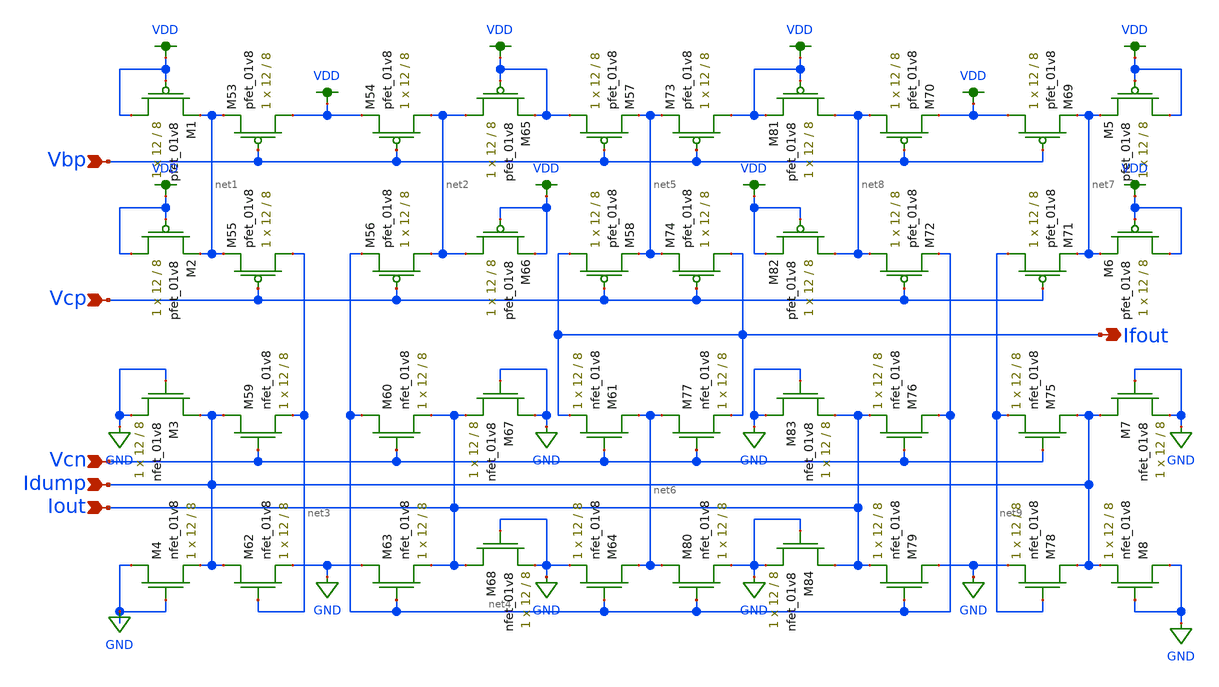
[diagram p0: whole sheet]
** sch_path: xschem/old_files/fvf.sch
**.subckt fvf Vbp Vcp Vcn Ifout Idump Iout
*.ipin Vbp
*.ipin Vcp
*.ipin Vcn
*.opin Ifout
*.ipin Idump
*.ipin Iout
XM53 VDD Vbp net1 VDD sky130_fd_pr__pfet_01v8 L=8 W=12 nf=1 ad='int((nf+1)/2) * W/nf * 0.29' as='int((nf+2)/2) * W/nf * 0.29'
+ pd='2*int((nf+1)/2) * (W/nf + 0.29)' ps='2*int((nf+2)/2) * (W/nf + 0.29)' nrd='0.29 / W' nrs='0.29 / W'
+ sa=0 sb=0 sd=0 mult=1 m=1
XM54 net2 Vbp VDD VDD sky130_fd_pr__pfet_01v8 L=8 W=12 nf=1 ad='int((nf+1)/2) * W/nf * 0.29' as='int((nf+2)/2) * W/nf * 0.29'
+ pd='2*int((nf+1)/2) * (W/nf + 0.29)' ps='2*int((nf+2)/2) * (W/nf + 0.29)' nrd='0.29 / W' nrs='0.29 / W'
+ sa=0 sb=0 sd=0 mult=1 m=1
XM55 net3 Vcp net1 VDD sky130_fd_pr__pfet_01v8 L=8 W=12 nf=1 ad='int((nf+1)/2) * W/nf * 0.29' as='int((nf+2)/2) * W/nf * 0.29'
+ pd='2*int((nf+1)/2) * (W/nf + 0.29)' ps='2*int((nf+2)/2) * (W/nf + 0.29)' nrd='0.29 / W' nrs='0.29 / W'
+ sa=0 sb=0 sd=0 mult=1 m=1
XM56 net2 Vcp net4 VDD sky130_fd_pr__pfet_01v8 L=8 W=12 nf=1 ad='int((nf+1)/2) * W/nf * 0.29' as='int((nf+2)/2) * W/nf * 0.29'
+ pd='2*int((nf+1)/2) * (W/nf + 0.29)' ps='2*int((nf+2)/2) * (W/nf + 0.29)' nrd='0.29 / W' nrs='0.29 / W'
+ sa=0 sb=0 sd=0 mult=1 m=1
XM57 VDD Vbp net5 VDD sky130_fd_pr__pfet_01v8 L=8 W=12 nf=1 ad='int((nf+1)/2) * W/nf * 0.29' as='int((nf+2)/2) * W/nf * 0.29'
+ pd='2*int((nf+1)/2) * (W/nf + 0.29)' ps='2*int((nf+2)/2) * (W/nf + 0.29)' nrd='0.29 / W' nrs='0.29 / W'
+ sa=0 sb=0 sd=0 mult=1 m=1
XM58 Ifout Vcp net5 VDD sky130_fd_pr__pfet_01v8 L=8 W=12 nf=1 ad='int((nf+1)/2) * W/nf * 0.29' as='int((nf+2)/2) * W/nf * 0.29'
+ pd='2*int((nf+1)/2) * (W/nf + 0.29)' ps='2*int((nf+2)/2) * (W/nf + 0.29)' nrd='0.29 / W' nrs='0.29 / W'
+ sa=0 sb=0 sd=0 mult=1 m=1
XM59 Idump Vcn net3 GND sky130_fd_pr__nfet_01v8 L=8 W=12 nf=1 ad='int((nf+1)/2) * W/nf * 0.29' as='int((nf+2)/2) * W/nf * 0.29'
+ pd='2*int((nf+1)/2) * (W/nf + 0.29)' ps='2*int((nf+2)/2) * (W/nf + 0.29)' nrd='0.29 / W' nrs='0.29 / W'
+ sa=0 sb=0 sd=0 mult=1 m=1
XM60 net4 Vcn Iout GND sky130_fd_pr__nfet_01v8 L=8 W=12 nf=1 ad='int((nf+1)/2) * W/nf * 0.29' as='int((nf+2)/2) * W/nf * 0.29'
+ pd='2*int((nf+1)/2) * (W/nf + 0.29)' ps='2*int((nf+2)/2) * (W/nf + 0.29)' nrd='0.29 / W' nrs='0.29 / W'
+ sa=0 sb=0 sd=0 mult=1 m=1
XM61 net6 Vcn Ifout GND sky130_fd_pr__nfet_01v8 L=8 W=12 nf=1 ad='int((nf+1)/2) * W/nf * 0.29' as='int((nf+2)/2) * W/nf * 0.29'
+ pd='2*int((nf+1)/2) * (W/nf + 0.29)' ps='2*int((nf+2)/2) * (W/nf + 0.29)' nrd='0.29 / W' nrs='0.29 / W'
+ sa=0 sb=0 sd=0 mult=1 m=1
XM62 Idump net3 GND GND sky130_fd_pr__nfet_01v8 L=8 W=12 nf=1 ad='int((nf+1)/2) * W/nf * 0.29' as='int((nf+2)/2) * W/nf * 0.29'
+ pd='2*int((nf+1)/2) * (W/nf + 0.29)' ps='2*int((nf+2)/2) * (W/nf + 0.29)' nrd='0.29 / W' nrs='0.29 / W'
+ sa=0 sb=0 sd=0 mult=1 m=1
XM63 GND net4 Iout GND sky130_fd_pr__nfet_01v8 L=8 W=12 nf=1 ad='int((nf+1)/2) * W/nf * 0.29' as='int((nf+2)/2) * W/nf * 0.29'
+ pd='2*int((nf+1)/2) * (W/nf + 0.29)' ps='2*int((nf+2)/2) * (W/nf + 0.29)' nrd='0.29 / W' nrs='0.29 / W'
+ sa=0 sb=0 sd=0 mult=1 m=1
XM64 net6 net4 GND GND sky130_fd_pr__nfet_01v8 L=8 W=12 nf=1 ad='int((nf+1)/2) * W/nf * 0.29' as='int((nf+2)/2) * W/nf * 0.29'
+ pd='2*int((nf+1)/2) * (W/nf + 0.29)' ps='2*int((nf+2)/2) * (W/nf + 0.29)' nrd='0.29 / W' nrs='0.29 / W'
+ sa=0 sb=0 sd=0 mult=1 m=1
XM65 net2 VDD VDD VDD sky130_fd_pr__pfet_01v8 L=8 W=12 nf=1 ad='int((nf+1)/2) * W/nf * 0.29' as='int((nf+2)/2) * W/nf * 0.29'
+ pd='2*int((nf+1)/2) * (W/nf + 0.29)' ps='2*int((nf+2)/2) * (W/nf + 0.29)' nrd='0.29 / W' nrs='0.29 / W'
+ sa=0 sb=0 sd=0 mult=1 m=1
XM66 net2 VDD VDD VDD sky130_fd_pr__pfet_01v8 L=8 W=12 nf=1 ad='int((nf+1)/2) * W/nf * 0.29' as='int((nf+2)/2) * W/nf * 0.29'
+ pd='2*int((nf+1)/2) * (W/nf + 0.29)' ps='2*int((nf+2)/2) * (W/nf + 0.29)' nrd='0.29 / W' nrs='0.29 / W'
+ sa=0 sb=0 sd=0 mult=1 m=1
XM67 GND GND Iout GND sky130_fd_pr__nfet_01v8 L=8 W=12 nf=1 ad='int((nf+1)/2) * W/nf * 0.29' as='int((nf+2)/2) * W/nf * 0.29'
+ pd='2*int((nf+1)/2) * (W/nf + 0.29)' ps='2*int((nf+2)/2) * (W/nf + 0.29)' nrd='0.29 / W' nrs='0.29 / W'
+ sa=0 sb=0 sd=0 mult=1 m=1
XM68 Iout GND GND GND sky130_fd_pr__nfet_01v8 L=8 W=12 nf=1 ad='int((nf+1)/2) * W/nf * 0.29' as='int((nf+2)/2) * W/nf * 0.29'
+ pd='2*int((nf+1)/2) * (W/nf + 0.29)' ps='2*int((nf+2)/2) * (W/nf + 0.29)' nrd='0.29 / W' nrs='0.29 / W'
+ sa=0 sb=0 sd=0 mult=1 m=1
XM69 VDD Vbp net7 VDD sky130_fd_pr__pfet_01v8 L=8 W=12 nf=1 ad='int((nf+1)/2) * W/nf * 0.29' as='int((nf+2)/2) * W/nf * 0.29'
+ pd='2*int((nf+1)/2) * (W/nf + 0.29)' ps='2*int((nf+2)/2) * (W/nf + 0.29)' nrd='0.29 / W' nrs='0.29 / W'
+ sa=0 sb=0 sd=0 mult=1 m=1
XM70 net8 Vbp VDD VDD sky130_fd_pr__pfet_01v8 L=8 W=12 nf=1 ad='int((nf+1)/2) * W/nf * 0.29' as='int((nf+2)/2) * W/nf * 0.29'
+ pd='2*int((nf+1)/2) * (W/nf + 0.29)' ps='2*int((nf+2)/2) * (W/nf + 0.29)' nrd='0.29 / W' nrs='0.29 / W'
+ sa=0 sb=0 sd=0 mult=1 m=1
XM71 net9 Vcp net7 VDD sky130_fd_pr__pfet_01v8 L=8 W=12 nf=1 ad='int((nf+1)/2) * W/nf * 0.29' as='int((nf+2)/2) * W/nf * 0.29'
+ pd='2*int((nf+1)/2) * (W/nf + 0.29)' ps='2*int((nf+2)/2) * (W/nf + 0.29)' nrd='0.29 / W' nrs='0.29 / W'
+ sa=0 sb=0 sd=0 mult=1 m=1
XM72 net8 Vcp net4 VDD sky130_fd_pr__pfet_01v8 L=8 W=12 nf=1 ad='int((nf+1)/2) * W/nf * 0.29' as='int((nf+2)/2) * W/nf * 0.29'
+ pd='2*int((nf+1)/2) * (W/nf + 0.29)' ps='2*int((nf+2)/2) * (W/nf + 0.29)' nrd='0.29 / W' nrs='0.29 / W'
+ sa=0 sb=0 sd=0 mult=1 m=1
XM73 VDD Vbp net5 VDD sky130_fd_pr__pfet_01v8 L=8 W=12 nf=1 ad='int((nf+1)/2) * W/nf * 0.29' as='int((nf+2)/2) * W/nf * 0.29'
+ pd='2*int((nf+1)/2) * (W/nf + 0.29)' ps='2*int((nf+2)/2) * (W/nf + 0.29)' nrd='0.29 / W' nrs='0.29 / W'
+ sa=0 sb=0 sd=0 mult=1 m=1
XM74 Ifout Vcp net5 VDD sky130_fd_pr__pfet_01v8 L=8 W=12 nf=1 ad='int((nf+1)/2) * W/nf * 0.29' as='int((nf+2)/2) * W/nf * 0.29'
+ pd='2*int((nf+1)/2) * (W/nf + 0.29)' ps='2*int((nf+2)/2) * (W/nf + 0.29)' nrd='0.29 / W' nrs='0.29 / W'
+ sa=0 sb=0 sd=0 mult=1 m=1
XM75 Idump Vcn net9 GND sky130_fd_pr__nfet_01v8 L=8 W=12 nf=1 ad='int((nf+1)/2) * W/nf * 0.29' as='int((nf+2)/2) * W/nf * 0.29'
+ pd='2*int((nf+1)/2) * (W/nf + 0.29)' ps='2*int((nf+2)/2) * (W/nf + 0.29)' nrd='0.29 / W' nrs='0.29 / W'
+ sa=0 sb=0 sd=0 mult=1 m=1
XM76 net4 Vcn Iout GND sky130_fd_pr__nfet_01v8 L=8 W=12 nf=1 ad='int((nf+1)/2) * W/nf * 0.29' as='int((nf+2)/2) * W/nf * 0.29'
+ pd='2*int((nf+1)/2) * (W/nf + 0.29)' ps='2*int((nf+2)/2) * (W/nf + 0.29)' nrd='0.29 / W' nrs='0.29 / W'
+ sa=0 sb=0 sd=0 mult=1 m=1
XM77 net6 Vcn Ifout GND sky130_fd_pr__nfet_01v8 L=8 W=12 nf=1 ad='int((nf+1)/2) * W/nf * 0.29' as='int((nf+2)/2) * W/nf * 0.29'
+ pd='2*int((nf+1)/2) * (W/nf + 0.29)' ps='2*int((nf+2)/2) * (W/nf + 0.29)' nrd='0.29 / W' nrs='0.29 / W'
+ sa=0 sb=0 sd=0 mult=1 m=1
XM78 Idump net9 GND GND sky130_fd_pr__nfet_01v8 L=8 W=12 nf=1 ad='int((nf+1)/2) * W/nf * 0.29' as='int((nf+2)/2) * W/nf * 0.29'
+ pd='2*int((nf+1)/2) * (W/nf + 0.29)' ps='2*int((nf+2)/2) * (W/nf + 0.29)' nrd='0.29 / W' nrs='0.29 / W'
+ sa=0 sb=0 sd=0 mult=1 m=1
XM79 GND net4 Iout GND sky130_fd_pr__nfet_01v8 L=8 W=12 nf=1 ad='int((nf+1)/2) * W/nf * 0.29' as='int((nf+2)/2) * W/nf * 0.29'
+ pd='2*int((nf+1)/2) * (W/nf + 0.29)' ps='2*int((nf+2)/2) * (W/nf + 0.29)' nrd='0.29 / W' nrs='0.29 / W'
+ sa=0 sb=0 sd=0 mult=1 m=1
XM80 net6 net4 GND GND sky130_fd_pr__nfet_01v8 L=8 W=12 nf=1 ad='int((nf+1)/2) * W/nf * 0.29' as='int((nf+2)/2) * W/nf * 0.29'
+ pd='2*int((nf+1)/2) * (W/nf + 0.29)' ps='2*int((nf+2)/2) * (W/nf + 0.29)' nrd='0.29 / W' nrs='0.29 / W'
+ sa=0 sb=0 sd=0 mult=1 m=1
XM81 net8 VDD VDD VDD sky130_fd_pr__pfet_01v8 L=8 W=12 nf=1 ad='int((nf+1)/2) * W/nf * 0.29' as='int((nf+2)/2) * W/nf * 0.29'
+ pd='2*int((nf+1)/2) * (W/nf + 0.29)' ps='2*int((nf+2)/2) * (W/nf + 0.29)' nrd='0.29 / W' nrs='0.29 / W'
+ sa=0 sb=0 sd=0 mult=1 m=1
XM82 net8 VDD VDD VDD sky130_fd_pr__pfet_01v8 L=8 W=12 nf=1 ad='int((nf+1)/2) * W/nf * 0.29' as='int((nf+2)/2) * W/nf * 0.29'
+ pd='2*int((nf+1)/2) * (W/nf + 0.29)' ps='2*int((nf+2)/2) * (W/nf + 0.29)' nrd='0.29 / W' nrs='0.29 / W'
+ sa=0 sb=0 sd=0 mult=1 m=1
XM83 GND GND Iout GND sky130_fd_pr__nfet_01v8 L=8 W=12 nf=1 ad='int((nf+1)/2) * W/nf * 0.29' as='int((nf+2)/2) * W/nf * 0.29'
+ pd='2*int((nf+1)/2) * (W/nf + 0.29)' ps='2*int((nf+2)/2) * (W/nf + 0.29)' nrd='0.29 / W' nrs='0.29 / W'
+ sa=0 sb=0 sd=0 mult=1 m=1
XM84 Iout GND GND GND sky130_fd_pr__nfet_01v8 L=8 W=12 nf=1 ad='int((nf+1)/2) * W/nf * 0.29' as='int((nf+2)/2) * W/nf * 0.29'
+ pd='2*int((nf+1)/2) * (W/nf + 0.29)' ps='2*int((nf+2)/2) * (W/nf + 0.29)' nrd='0.29 / W' nrs='0.29 / W'
+ sa=0 sb=0 sd=0 mult=1 m=1
XM1 VDD VDD net1 VDD sky130_fd_pr__pfet_01v8 L=8 W=12 nf=1 ad='int((nf+1)/2) * W/nf * 0.29' as='int((nf+2)/2) * W/nf * 0.29'
+ pd='2*int((nf+1)/2) * (W/nf + 0.29)' ps='2*int((nf+2)/2) * (W/nf + 0.29)' nrd='0.29 / W' nrs='0.29 / W'
+ sa=0 sb=0 sd=0 mult=1 m=1
XM2 VDD VDD net1 VDD sky130_fd_pr__pfet_01v8 L=8 W=12 nf=1 ad='int((nf+1)/2) * W/nf * 0.29' as='int((nf+2)/2) * W/nf * 0.29'
+ pd='2*int((nf+1)/2) * (W/nf + 0.29)' ps='2*int((nf+2)/2) * (W/nf + 0.29)' nrd='0.29 / W' nrs='0.29 / W'
+ sa=0 sb=0 sd=0 mult=1 m=1
XM3 Idump GND GND GND sky130_fd_pr__nfet_01v8 L=8 W=12 nf=1 ad='int((nf+1)/2) * W/nf * 0.29' as='int((nf+2)/2) * W/nf * 0.29'
+ pd='2*int((nf+1)/2) * (W/nf + 0.29)' ps='2*int((nf+2)/2) * (W/nf + 0.29)' nrd='0.29 / W' nrs='0.29 / W'
+ sa=0 sb=0 sd=0 mult=1 m=1
XM4 GND GND Idump GND sky130_fd_pr__nfet_01v8 L=8 W=12 nf=1 ad='int((nf+1)/2) * W/nf * 0.29' as='int((nf+2)/2) * W/nf * 0.29'
+ pd='2*int((nf+1)/2) * (W/nf + 0.29)' ps='2*int((nf+2)/2) * (W/nf + 0.29)' nrd='0.29 / W' nrs='0.29 / W'
+ sa=0 sb=0 sd=0 mult=1 m=1
XM5 VDD VDD net7 VDD sky130_fd_pr__pfet_01v8 L=8 W=12 nf=1 ad='int((nf+1)/2) * W/nf * 0.29' as='int((nf+2)/2) * W/nf * 0.29'
+ pd='2*int((nf+1)/2) * (W/nf + 0.29)' ps='2*int((nf+2)/2) * (W/nf + 0.29)' nrd='0.29 / W' nrs='0.29 / W'
+ sa=0 sb=0 sd=0 mult=1 m=1
XM6 VDD VDD net7 VDD sky130_fd_pr__pfet_01v8 L=8 W=12 nf=1 ad='int((nf+1)/2) * W/nf * 0.29' as='int((nf+2)/2) * W/nf * 0.29'
+ pd='2*int((nf+1)/2) * (W/nf + 0.29)' ps='2*int((nf+2)/2) * (W/nf + 0.29)' nrd='0.29 / W' nrs='0.29 / W'
+ sa=0 sb=0 sd=0 mult=1 m=1
XM7 Idump GND GND GND sky130_fd_pr__nfet_01v8 L=8 W=12 nf=1 ad='int((nf+1)/2) * W/nf * 0.29' as='int((nf+2)/2) * W/nf * 0.29'
+ pd='2*int((nf+1)/2) * (W/nf + 0.29)' ps='2*int((nf+2)/2) * (W/nf + 0.29)' nrd='0.29 / W' nrs='0.29 / W'
+ sa=0 sb=0 sd=0 mult=1 m=1
XM8 GND GND Idump GND sky130_fd_pr__nfet_01v8 L=8 W=12 nf=1 ad='int((nf+1)/2) * W/nf * 0.29' as='int((nf+2)/2) * W/nf * 0.29'
+ pd='2*int((nf+1)/2) * (W/nf + 0.29)' ps='2*int((nf+2)/2) * (W/nf + 0.29)' nrd='0.29 / W' nrs='0.29 / W'
+ sa=0 sb=0 sd=0 mult=1 m=1
**.ends
.GLOBAL VDD
.GLOBAL GND
.end
